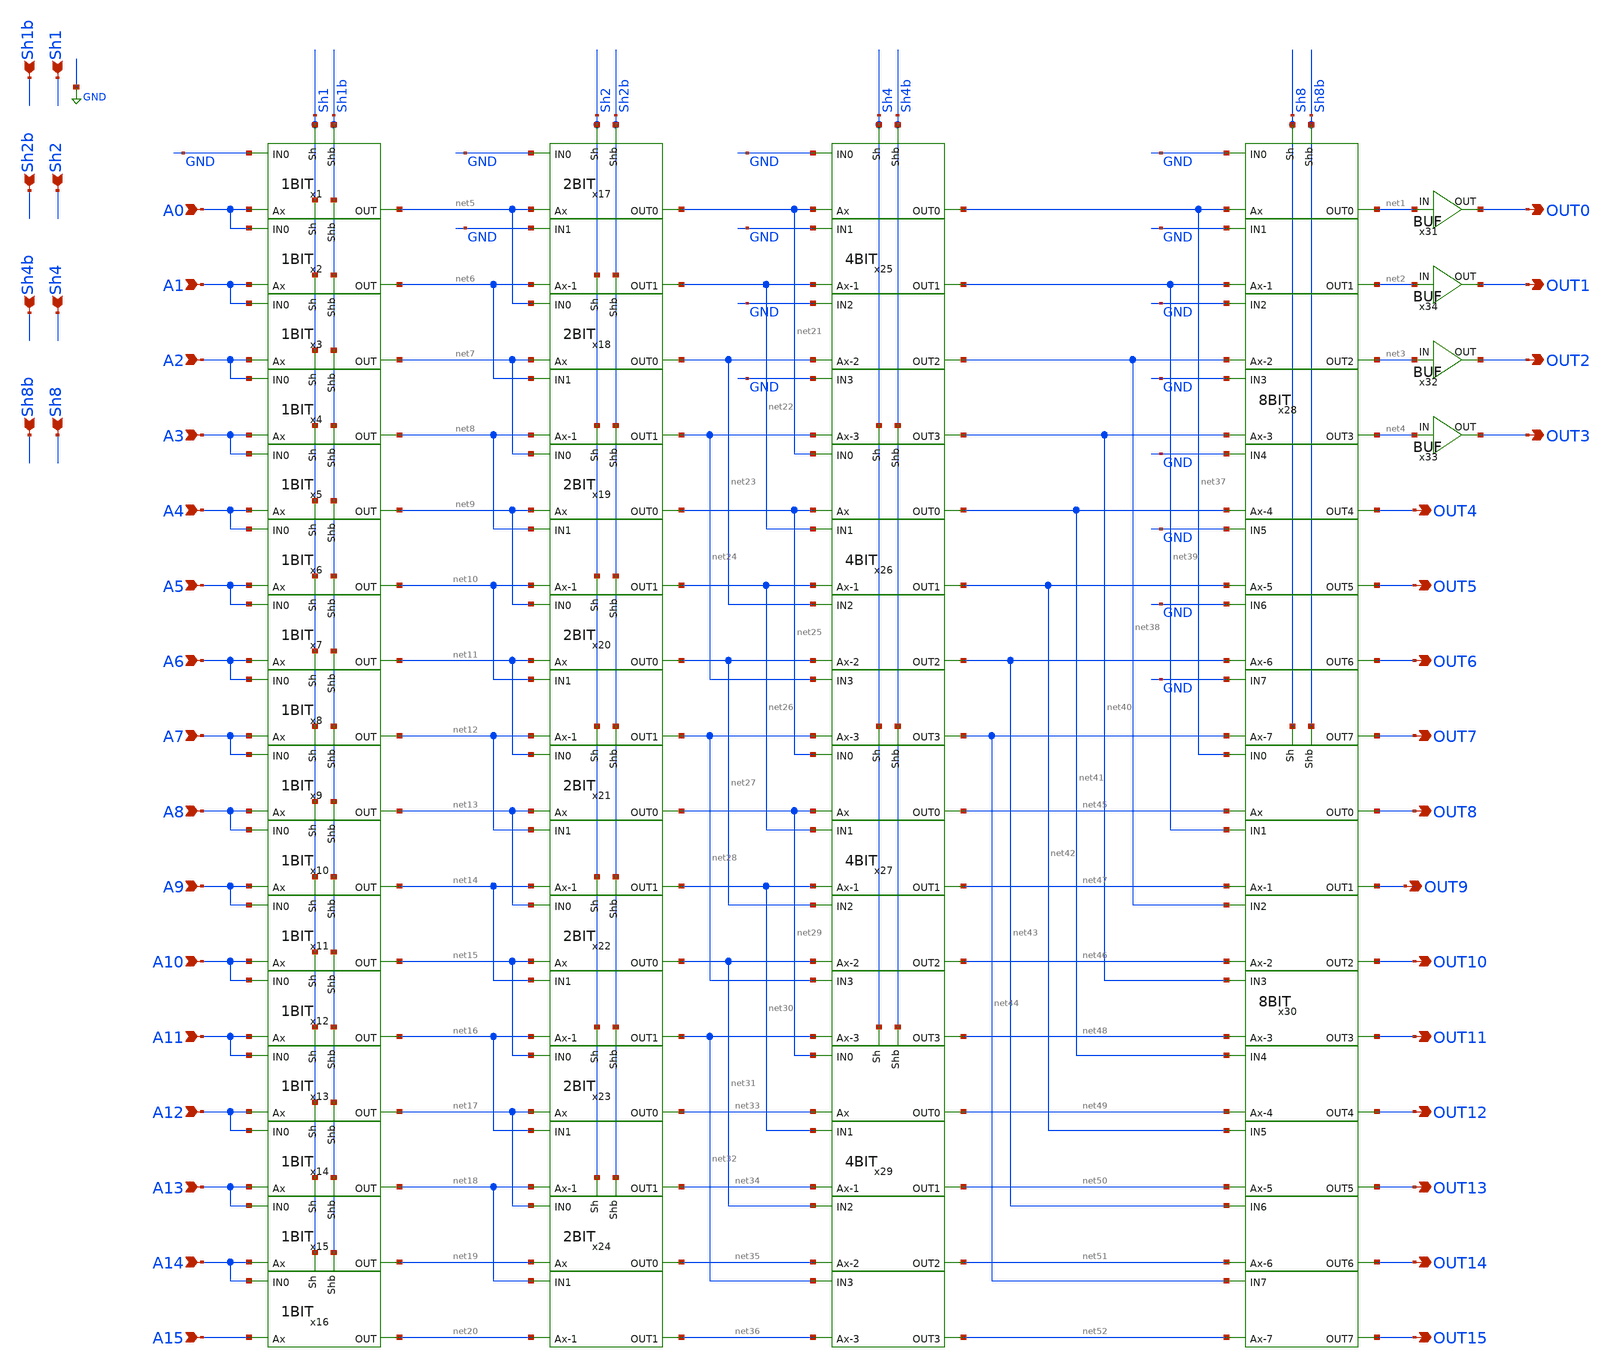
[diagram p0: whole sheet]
** sch_path: SHIFT.sch
**.subckt SHIFT Sh1 Sh1b A0 A1 A2 A3 A4 A5 A6 A7 A8 A9 A10 A11 A12 A13 A14 A15 OUT0 OUT1 OUT2 OUT3
*+ OUT4 OUT5 OUT6 OUT7 OUT8 OUT9 OUT10 OUT11 OUT12 OUT13 OUT14 OUT15 Sh2 Sh2b Sh4 Sh4b Sh8 Sh8b
*.ipin Sh1
*.ipin Sh1b
*.ipin A0
*.ipin A1
*.ipin A2
*.ipin A3
*.ipin A4
*.ipin A5
*.ipin A6
*.ipin A7
*.ipin A8
*.ipin A9
*.ipin A10
*.ipin A11
*.ipin A12
*.ipin A13
*.ipin A14
*.ipin A15
*.opin OUT0
*.opin OUT1
*.opin OUT2
*.opin OUT3
*.opin OUT4
*.opin OUT5
*.opin OUT6
*.opin OUT7
*.opin OUT8
*.opin OUT9
*.opin OUT10
*.opin OUT11
*.opin OUT12
*.opin OUT13
*.opin OUT14
*.opin OUT15
*.ipin Sh2
*.ipin Sh2b
*.ipin Sh4
*.ipin Sh4b
*.ipin Sh8
*.ipin Sh8b
x1 Sh1b Sh1 A0 GND net5 1BIT
x2 Sh1b Sh1 A1 A0 net6 1BIT
x3 Sh1b Sh1 A2 A1 net7 1BIT
x4 Sh1b Sh1 A3 A2 net8 1BIT
x5 Sh1b Sh1 A4 A3 net9 1BIT
x6 Sh1b Sh1 A5 A4 net10 1BIT
x7 Sh1b Sh1 A6 A5 net11 1BIT
x8 Sh1b Sh1 A7 A6 net12 1BIT
x9 Sh1b Sh1 A8 A7 net13 1BIT
x10 Sh1b Sh1 A9 A8 net14 1BIT
x11 Sh1b Sh1 A10 A9 net15 1BIT
x12 Sh1b Sh1 A11 A10 net16 1BIT
x13 Sh1b Sh1 A12 A11 net17 1BIT
x14 Sh1b Sh1 A13 A12 net18 1BIT
x15 Sh1b Sh1 A14 A13 net19 1BIT
x16 Sh1b Sh1 A15 A14 net20 1BIT
x17 Sh2b Sh2 net5 GND net21 net22 GND net6 2BIT
x18 Sh2b Sh2 net7 net5 net23 net24 net6 net8 2BIT
x19 Sh2b Sh2 net9 net7 net25 net26 net8 net10 2BIT
x20 Sh2b Sh2 net11 net9 net27 net28 net10 net12 2BIT
x21 Sh2b Sh2 net13 net11 net29 net30 net12 net14 2BIT
x22 Sh2b Sh2 net15 net13 net31 net32 net14 net16 2BIT
x23 Sh2b Sh2 net17 net15 net33 net34 net16 net18 2BIT
x24 Sh2b Sh2 net19 net17 net35 net36 net18 net20 2BIT
x25 Sh4b Sh4 GND net21 net37 net39 net38 net40 GND net22 GND net23 GND net24 4BIT
x26 Sh4b Sh4 net21 net25 net41 net42 net43 net44 net22 net26 net23 net27 net24 net28 4BIT
x27 Sh4b Sh4 net25 net29 net45 net47 net46 net48 net26 net30 net27 net31 net28 net32 4BIT
x29 Sh4b Sh4 net29 net33 net49 net50 net51 net52 net30 net34 net31 net35 net32 net36 4BIT
x28 Sh8b Sh8 net37 GND net1 net2 net3 net4 net39 GND GND net38 GND net40 net41 GND OUT4 OUT5 OUT6
+ OUT7 GND net42 GND net43 GND net44 8BIT
x30 Sh8b Sh8 net45 net37 OUT8 OUT9 OUT10 OUT11 net47 net39 net38 net46 net40 net48 net49 net41 OUT12
+ OUT13 OUT14 OUT15 net42 net50 net43 net51 net44 net52 8BIT
x31 OUT0 net1 BUF
x32 OUT2 net3 BUF
x33 OUT3 net4 BUF
x34 OUT1 net2 BUF
**.ends
.GLOBAL GND
.end
